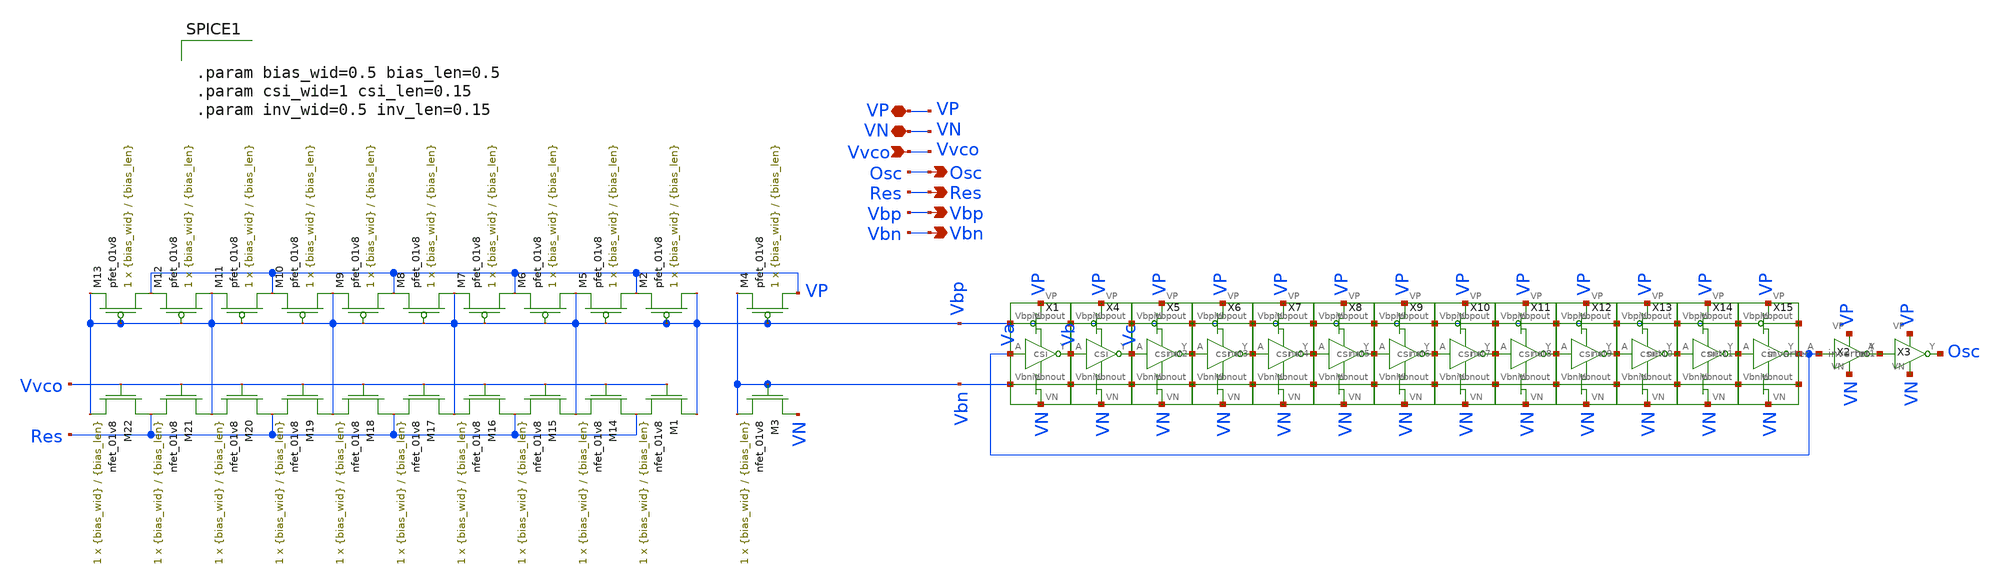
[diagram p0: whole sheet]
** sch_path: LDS/LDS_vco.sch
**.subckt LDS_vco VN VP Osc Vvco Res Vbp Vbn
*.iopin VN
*.iopin VP
*.opin Osc
*.ipin Vvco
*.opin Res
*.opin Vbp
*.opin Vbn
XM3 VN Vbn Vbn VN sky130_fd_pr__nfet_01v8 L={bias_len} W={bias_wid} nf=1 ad='int((nf+1)/2) * W/nf * 0.29'
+ as='int((nf+2)/2) * W/nf * 0.29' pd='2*int((nf+1)/2) * (W/nf + 0.29)' ps='2*int((nf+2)/2) * (W/nf + 0.29)'
+ nrd='0.29 / W' nrs='0.29 / W' sa=0 sb=0 sd=0 mult=1 m=1
XM4 VP Vbp Vbn VP sky130_fd_pr__pfet_01v8 L={bias_len} W={bias_wid} nf=1 ad='int((nf+1)/2) * W/nf * 0.29'
+ as='int((nf+2)/2) * W/nf * 0.29' pd='2*int((nf+1)/2) * (W/nf + 0.29)' ps='2*int((nf+2)/2) * (W/nf + 0.29)'
+ nrd='0.29 / W' nrs='0.29 / W' sa=0 sb=0 sd=0 mult=1 m=1
XM1 Vbp Vvco Res VN sky130_fd_pr__nfet_01v8 L={bias_len} W={bias_wid} nf=1 ad='int((nf+1)/2) * W/nf * 0.29'
+ as='int((nf+2)/2) * W/nf * 0.29' pd='2*int((nf+1)/2) * (W/nf + 0.29)' ps='2*int((nf+2)/2) * (W/nf + 0.29)'
+ nrd='0.29 / W' nrs='0.29 / W' sa=0 sb=0 sd=0 mult=1 m=1
XM2 Vbp Vbp VP VP sky130_fd_pr__pfet_01v8 L={bias_len} W={bias_wid} nf=1 ad='int((nf+1)/2) * W/nf * 0.29'
+ as='int((nf+2)/2) * W/nf * 0.29' pd='2*int((nf+1)/2) * (W/nf + 0.29)' ps='2*int((nf+2)/2) * (W/nf + 0.29)'
+ nrd='0.29 / W' nrs='0.29 / W' sa=0 sb=0 sd=0 mult=1 m=1
X2 Va net1 VP VN inverter
X3 net1 Osc VP VN inverter
X1 VP VN Va Vb Vbp Vbn Vbp Vbn csi
X4 VP VN Vb Vc Vbp Vbn Vbp Vbn csi
X5 VP VN Vc net2 Vbp Vbn Vbp Vbn csi
X6 VP VN net2 net3 Vbp Vbn Vbp Vbn csi
X7 VP VN net3 net4 Vbp Vbn Vbp Vbn csi
X8 VP VN net4 net5 Vbp Vbn Vbp Vbn csi
X9 VP VN net5 net6 Vbp Vbn Vbp Vbn csi
X10 VP VN net6 net7 Vbp Vbn Vbp Vbn csi
X11 VP VN net7 net8 Vbp Vbn Vbp Vbn csi
X12 VP VN net8 net9 Vbp Vbn Vbp Vbn csi
X13 VP VN net9 net10 Vbp Vbn Vbp Vbn csi
X14 VP VN net10 net11 Vbp Vbn Vbp Vbn csi
X15 VP VN net11 Va Vbp Vbn net12 net13 csi
XM5 VP Vbp Vbp VP sky130_fd_pr__pfet_01v8 L={bias_len} W={bias_wid} nf=1 ad='int((nf+1)/2) * W/nf * 0.29'
+ as='int((nf+2)/2) * W/nf * 0.29' pd='2*int((nf+1)/2) * (W/nf + 0.29)' ps='2*int((nf+2)/2) * (W/nf + 0.29)'
+ nrd='0.29 / W' nrs='0.29 / W' sa=0 sb=0 sd=0 mult=1 m=1
XM6 Vbp Vbp VP VP sky130_fd_pr__pfet_01v8 L={bias_len} W={bias_wid} nf=1 ad='int((nf+1)/2) * W/nf * 0.29'
+ as='int((nf+2)/2) * W/nf * 0.29' pd='2*int((nf+1)/2) * (W/nf + 0.29)' ps='2*int((nf+2)/2) * (W/nf + 0.29)'
+ nrd='0.29 / W' nrs='0.29 / W' sa=0 sb=0 sd=0 mult=1 m=1
XM7 VP Vbp Vbp VP sky130_fd_pr__pfet_01v8 L={bias_len} W={bias_wid} nf=1 ad='int((nf+1)/2) * W/nf * 0.29'
+ as='int((nf+2)/2) * W/nf * 0.29' pd='2*int((nf+1)/2) * (W/nf + 0.29)' ps='2*int((nf+2)/2) * (W/nf + 0.29)'
+ nrd='0.29 / W' nrs='0.29 / W' sa=0 sb=0 sd=0 mult=1 m=1
XM8 Vbp Vbp VP VP sky130_fd_pr__pfet_01v8 L={bias_len} W={bias_wid} nf=1 ad='int((nf+1)/2) * W/nf * 0.29'
+ as='int((nf+2)/2) * W/nf * 0.29' pd='2*int((nf+1)/2) * (W/nf + 0.29)' ps='2*int((nf+2)/2) * (W/nf + 0.29)'
+ nrd='0.29 / W' nrs='0.29 / W' sa=0 sb=0 sd=0 mult=1 m=1
XM9 VP Vbp Vbp VP sky130_fd_pr__pfet_01v8 L={bias_len} W={bias_wid} nf=1 ad='int((nf+1)/2) * W/nf * 0.29'
+ as='int((nf+2)/2) * W/nf * 0.29' pd='2*int((nf+1)/2) * (W/nf + 0.29)' ps='2*int((nf+2)/2) * (W/nf + 0.29)'
+ nrd='0.29 / W' nrs='0.29 / W' sa=0 sb=0 sd=0 mult=1 m=1
XM10 Vbp Vbp VP VP sky130_fd_pr__pfet_01v8 L={bias_len} W={bias_wid} nf=1 ad='int((nf+1)/2) * W/nf * 0.29'
+ as='int((nf+2)/2) * W/nf * 0.29' pd='2*int((nf+1)/2) * (W/nf + 0.29)' ps='2*int((nf+2)/2) * (W/nf + 0.29)'
+ nrd='0.29 / W' nrs='0.29 / W' sa=0 sb=0 sd=0 mult=1 m=1
XM11 VP Vbp Vbp VP sky130_fd_pr__pfet_01v8 L={bias_len} W={bias_wid} nf=1 ad='int((nf+1)/2) * W/nf * 0.29'
+ as='int((nf+2)/2) * W/nf * 0.29' pd='2*int((nf+1)/2) * (W/nf + 0.29)' ps='2*int((nf+2)/2) * (W/nf + 0.29)'
+ nrd='0.29 / W' nrs='0.29 / W' sa=0 sb=0 sd=0 mult=1 m=1
XM12 Vbp Vbp VP VP sky130_fd_pr__pfet_01v8 L={bias_len} W={bias_wid} nf=1 ad='int((nf+1)/2) * W/nf * 0.29'
+ as='int((nf+2)/2) * W/nf * 0.29' pd='2*int((nf+1)/2) * (W/nf + 0.29)' ps='2*int((nf+2)/2) * (W/nf + 0.29)'
+ nrd='0.29 / W' nrs='0.29 / W' sa=0 sb=0 sd=0 mult=1 m=1
XM13 VP Vbp Vbp VP sky130_fd_pr__pfet_01v8 L={bias_len} W={bias_wid} nf=1 ad='int((nf+1)/2) * W/nf * 0.29'
+ as='int((nf+2)/2) * W/nf * 0.29' pd='2*int((nf+1)/2) * (W/nf + 0.29)' ps='2*int((nf+2)/2) * (W/nf + 0.29)'
+ nrd='0.29 / W' nrs='0.29 / W' sa=0 sb=0 sd=0 mult=1 m=1
XM14 Res Vvco Vbp VN sky130_fd_pr__nfet_01v8 L={bias_len} W={bias_wid} nf=1 ad='int((nf+1)/2) * W/nf * 0.29'
+ as='int((nf+2)/2) * W/nf * 0.29' pd='2*int((nf+1)/2) * (W/nf + 0.29)' ps='2*int((nf+2)/2) * (W/nf + 0.29)'
+ nrd='0.29 / W' nrs='0.29 / W' sa=0 sb=0 sd=0 mult=1 m=1
XM15 Vbp Vvco Res VN sky130_fd_pr__nfet_01v8 L={bias_len} W={bias_wid} nf=1 ad='int((nf+1)/2) * W/nf * 0.29'
+ as='int((nf+2)/2) * W/nf * 0.29' pd='2*int((nf+1)/2) * (W/nf + 0.29)' ps='2*int((nf+2)/2) * (W/nf + 0.29)'
+ nrd='0.29 / W' nrs='0.29 / W' sa=0 sb=0 sd=0 mult=1 m=1
XM16 Res Vvco Vbp VN sky130_fd_pr__nfet_01v8 L={bias_len} W={bias_wid} nf=1 ad='int((nf+1)/2) * W/nf * 0.29'
+ as='int((nf+2)/2) * W/nf * 0.29' pd='2*int((nf+1)/2) * (W/nf + 0.29)' ps='2*int((nf+2)/2) * (W/nf + 0.29)'
+ nrd='0.29 / W' nrs='0.29 / W' sa=0 sb=0 sd=0 mult=1 m=1
XM17 Vbp Vvco Res VN sky130_fd_pr__nfet_01v8 L={bias_len} W={bias_wid} nf=1 ad='int((nf+1)/2) * W/nf * 0.29'
+ as='int((nf+2)/2) * W/nf * 0.29' pd='2*int((nf+1)/2) * (W/nf + 0.29)' ps='2*int((nf+2)/2) * (W/nf + 0.29)'
+ nrd='0.29 / W' nrs='0.29 / W' sa=0 sb=0 sd=0 mult=1 m=1
XM18 Res Vvco Vbp VN sky130_fd_pr__nfet_01v8 L={bias_len} W={bias_wid} nf=1 ad='int((nf+1)/2) * W/nf * 0.29'
+ as='int((nf+2)/2) * W/nf * 0.29' pd='2*int((nf+1)/2) * (W/nf + 0.29)' ps='2*int((nf+2)/2) * (W/nf + 0.29)'
+ nrd='0.29 / W' nrs='0.29 / W' sa=0 sb=0 sd=0 mult=1 m=1
XM19 Vbp Vvco Res VN sky130_fd_pr__nfet_01v8 L={bias_len} W={bias_wid} nf=1 ad='int((nf+1)/2) * W/nf * 0.29'
+ as='int((nf+2)/2) * W/nf * 0.29' pd='2*int((nf+1)/2) * (W/nf + 0.29)' ps='2*int((nf+2)/2) * (W/nf + 0.29)'
+ nrd='0.29 / W' nrs='0.29 / W' sa=0 sb=0 sd=0 mult=1 m=1
XM20 Res Vvco Vbp VN sky130_fd_pr__nfet_01v8 L={bias_len} W={bias_wid} nf=1 ad='int((nf+1)/2) * W/nf * 0.29'
+ as='int((nf+2)/2) * W/nf * 0.29' pd='2*int((nf+1)/2) * (W/nf + 0.29)' ps='2*int((nf+2)/2) * (W/nf + 0.29)'
+ nrd='0.29 / W' nrs='0.29 / W' sa=0 sb=0 sd=0 mult=1 m=1
XM21 Vbp Vvco Res VN sky130_fd_pr__nfet_01v8 L={bias_len} W={bias_wid} nf=1 ad='int((nf+1)/2) * W/nf * 0.29'
+ as='int((nf+2)/2) * W/nf * 0.29' pd='2*int((nf+1)/2) * (W/nf + 0.29)' ps='2*int((nf+2)/2) * (W/nf + 0.29)'
+ nrd='0.29 / W' nrs='0.29 / W' sa=0 sb=0 sd=0 mult=1 m=1
XM22 Res Vvco Vbp VN sky130_fd_pr__nfet_01v8 L={bias_len} W={bias_wid} nf=1 ad='int((nf+1)/2) * W/nf * 0.29'
+ as='int((nf+2)/2) * W/nf * 0.29' pd='2*int((nf+1)/2) * (W/nf + 0.29)' ps='2*int((nf+2)/2) * (W/nf + 0.29)'
+ nrd='0.29 / W' nrs='0.29 / W' sa=0 sb=0 sd=0 mult=1 m=1
**** begin user architecture code


.param bias_wid=0.5 bias_len=0.5
.param csi_wid=1 csi_len=0.15
.param inv_wid=0.5 inv_len=0.15


**** end user architecture code
**.ends

* expanding   symbol:  inverter.sym # of pins=4
** sym_path: LDS/inverter.sym
** sch_path: LDS/inverter.sch
.subckt inverter A Y VP VN
*.iopin VP
*.ipin A
*.opin Y
*.iopin VN
XM2 Y A VP VP sky130_fd_pr__pfet_01v8 L={inv_len} W={inv_wid} nf=1 ad='int((nf+1)/2) * W/nf * 0.29' as='int((nf+2)/2) * W/nf * 0.29'
+ pd='2*int((nf+1)/2) * (W/nf + 0.29)' ps='2*int((nf+2)/2) * (W/nf + 0.29)' nrd='0.29 / W' nrs='0.29 / W'
+ sa=0 sb=0 sd=0 mult=1 m=1
XM1 Y A VN VN sky130_fd_pr__nfet_01v8 L={inv_len} W={inv_wid} nf=1 ad='int((nf+1)/2) * W/nf * 0.29' as='int((nf+2)/2) * W/nf * 0.29'
+ pd='2*int((nf+1)/2) * (W/nf + 0.29)' ps='2*int((nf+2)/2) * (W/nf + 0.29)' nrd='0.29 / W' nrs='0.29 / W'
+ sa=0 sb=0 sd=0 mult=1 m=1
.ends


* expanding   symbol:  csi.sym # of pins=8
** sym_path: LDS/csi.sym
** sch_path: LDS/csi.sch
.subckt csi VP VN A Y Vbpin Vbnin Vbpout Vbnout
*.iopin VN
*.iopin VP
*.opin Y
*.ipin Vbpin
*.ipin A
*.ipin Vbnin
*.opin Vbpout
*.opin Vbnout
XM1 Y A net1 VN sky130_fd_pr__nfet_01v8 L={csi_len} W={csi_wid} nf=1 ad='int((nf+1)/2) * W/nf * 0.29'
+ as='int((nf+2)/2) * W/nf * 0.29' pd='2*int((nf+1)/2) * (W/nf + 0.29)' ps='2*int((nf+2)/2) * (W/nf + 0.29)'
+ nrd='0.29 / W' nrs='0.29 / W' sa=0 sb=0 sd=0 mult=1 m=1
XM2 Y A net2 VP sky130_fd_pr__pfet_01v8 L={csi_len} W={csi_wid} nf=1 ad='int((nf+1)/2) * W/nf * 0.29'
+ as='int((nf+2)/2) * W/nf * 0.29' pd='2*int((nf+1)/2) * (W/nf + 0.29)' ps='2*int((nf+2)/2) * (W/nf + 0.29)'
+ nrd='0.29 / W' nrs='0.29 / W' sa=0 sb=0 sd=0 mult=1 m=1
XM3 net1 Vbnin VN VN sky130_fd_pr__nfet_01v8 L={bias_len} W={bias_wid} nf=1 ad='int((nf+1)/2) * W/nf * 0.29'
+ as='int((nf+2)/2) * W/nf * 0.29' pd='2*int((nf+1)/2) * (W/nf + 0.29)' ps='2*int((nf+2)/2) * (W/nf + 0.29)'
+ nrd='0.29 / W' nrs='0.29 / W' sa=0 sb=0 sd=0 mult=1 m=1
XM4 net2 Vbpin VP VP sky130_fd_pr__pfet_01v8 L={bias_len} W={bias_wid} nf=1 ad='int((nf+1)/2) * W/nf * 0.29'
+ as='int((nf+2)/2) * W/nf * 0.29' pd='2*int((nf+1)/2) * (W/nf + 0.29)' ps='2*int((nf+2)/2) * (W/nf + 0.29)'
+ nrd='0.29 / W' nrs='0.29 / W' sa=0 sb=0 sd=0 mult=1 m=1
Vm1 Vbpin Vbpout 0
.save i(vm1)
Vm2 Vbnin Vbnout 0
.save i(vm2)
.ends

.end
